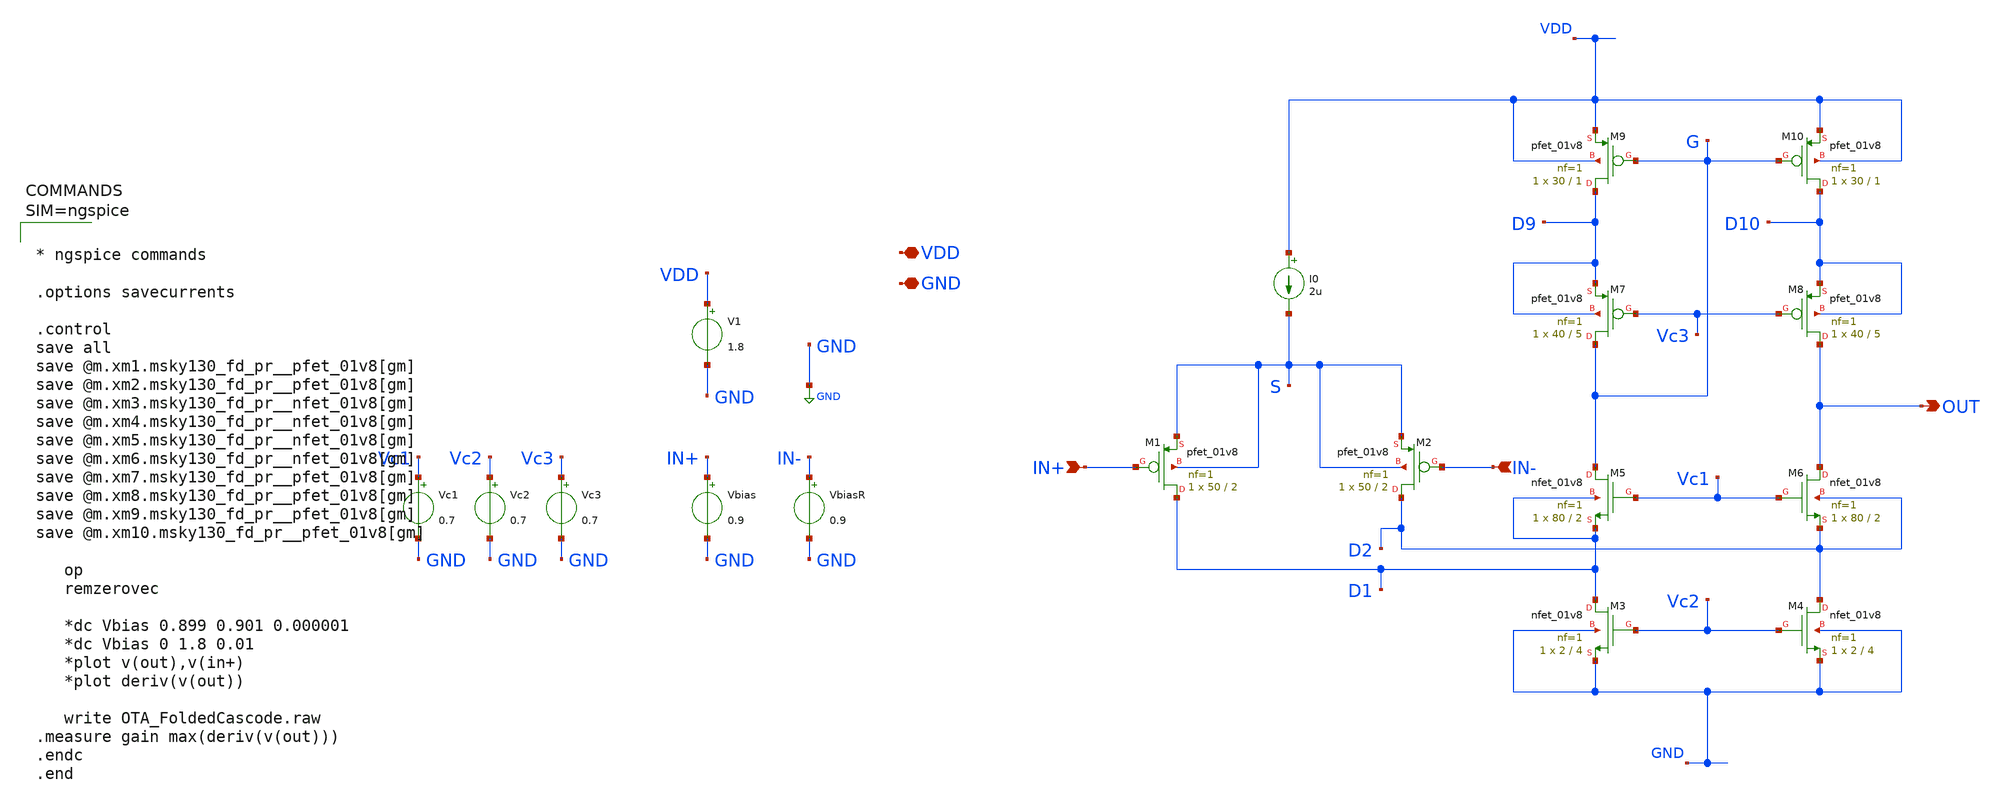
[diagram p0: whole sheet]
** sch_path: xschem/OTA_FoldedCascode.sch
**.subckt OTA_FoldedCascode VDD GND IN+ IN- OUT
*.iopin VDD
*.iopin GND
*.ipin IN+
*.ipin IN-
*.opin OUT
V1 VDD GND 1.8
Vbias IN+ GND 0.9
VbiasR IN- GND 0.9
I0 VDD S 2u
XM1 D1 IN+ S S sky130_fd_pr__pfet_01v8 L=2 W=50 nf=1 ad='int((nf+1)/2) * W/nf * 0.29' as='int((nf+2)/2) * W/nf * 0.29'
+ pd='2*int((nf+1)/2) * (W/nf + 0.29)' ps='2*int((nf+2)/2) * (W/nf + 0.29)' nrd='0.29 / W' nrs='0.29 / W'
+ sa=0 sb=0 sd=0 mult=1 m=1
XM2 D2 IN- S S sky130_fd_pr__pfet_01v8 L=2 W=50 nf=1 ad='int((nf+1)/2) * W/nf * 0.29' as='int((nf+2)/2) * W/nf * 0.29'
+ pd='2*int((nf+1)/2) * (W/nf + 0.29)' ps='2*int((nf+2)/2) * (W/nf + 0.29)' nrd='0.29 / W' nrs='0.29 / W'
+ sa=0 sb=0 sd=0 mult=1 m=1
XM3 D1 Vc2 GND GND sky130_fd_pr__nfet_01v8 L=4 W=2 nf=1 ad='int((nf+1)/2) * W/nf * 0.29' as='int((nf+2)/2) * W/nf * 0.29'
+ pd='2*int((nf+1)/2) * (W/nf + 0.29)' ps='2*int((nf+2)/2) * (W/nf + 0.29)' nrd='0.29 / W' nrs='0.29 / W'
+ sa=0 sb=0 sd=0 mult=1 m=1
XM4 D2 Vc2 GND GND sky130_fd_pr__nfet_01v8 L=4 W=2 nf=1 ad='int((nf+1)/2) * W/nf * 0.29' as='int((nf+2)/2) * W/nf * 0.29'
+ pd='2*int((nf+1)/2) * (W/nf + 0.29)' ps='2*int((nf+2)/2) * (W/nf + 0.29)' nrd='0.29 / W' nrs='0.29 / W'
+ sa=0 sb=0 sd=0 mult=1 m=1
XM5 G Vc1 D1 D1 sky130_fd_pr__nfet_01v8 L=2 W=80 nf=1 ad='int((nf+1)/2) * W/nf * 0.29' as='int((nf+2)/2) * W/nf * 0.29'
+ pd='2*int((nf+1)/2) * (W/nf + 0.29)' ps='2*int((nf+2)/2) * (W/nf + 0.29)' nrd='0.29 / W' nrs='0.29 / W'
+ sa=0 sb=0 sd=0 mult=1 m=1
XM6 OUT Vc1 D2 D2 sky130_fd_pr__nfet_01v8 L=2 W=80 nf=1 ad='int((nf+1)/2) * W/nf * 0.29' as='int((nf+2)/2) * W/nf * 0.29'
+ pd='2*int((nf+1)/2) * (W/nf + 0.29)' ps='2*int((nf+2)/2) * (W/nf + 0.29)' nrd='0.29 / W' nrs='0.29 / W'
+ sa=0 sb=0 sd=0 mult=1 m=1
XM7 G Vc3 D9 D9 sky130_fd_pr__pfet_01v8 L=5 W=40 nf=1 ad='int((nf+1)/2) * W/nf * 0.29' as='int((nf+2)/2) * W/nf * 0.29'
+ pd='2*int((nf+1)/2) * (W/nf + 0.29)' ps='2*int((nf+2)/2) * (W/nf + 0.29)' nrd='0.29 / W' nrs='0.29 / W'
+ sa=0 sb=0 sd=0 mult=1 m=1
XM8 OUT Vc3 D10 D10 sky130_fd_pr__pfet_01v8 L=5 W=40 nf=1 ad='int((nf+1)/2) * W/nf * 0.29' as='int((nf+2)/2) * W/nf * 0.29'
+ pd='2*int((nf+1)/2) * (W/nf + 0.29)' ps='2*int((nf+2)/2) * (W/nf + 0.29)' nrd='0.29 / W' nrs='0.29 / W'
+ sa=0 sb=0 sd=0 mult=1 m=1
XM9 D9 G VDD VDD sky130_fd_pr__pfet_01v8 L=1 W=30 nf=1 ad='int((nf+1)/2) * W/nf * 0.29' as='int((nf+2)/2) * W/nf * 0.29'
+ pd='2*int((nf+1)/2) * (W/nf + 0.29)' ps='2*int((nf+2)/2) * (W/nf + 0.29)' nrd='0.29 / W' nrs='0.29 / W'
+ sa=0 sb=0 sd=0 mult=1 m=1
XM10 D10 G VDD VDD sky130_fd_pr__pfet_01v8 L=1 W=30 nf=1 ad='int((nf+1)/2) * W/nf * 0.29' as='int((nf+2)/2) * W/nf * 0.29'
+ pd='2*int((nf+1)/2) * (W/nf + 0.29)' ps='2*int((nf+2)/2) * (W/nf + 0.29)' nrd='0.29 / W' nrs='0.29 / W'
+ sa=0 sb=0 sd=0 mult=1 m=1
Vc1 Vc1 GND 0.7
Vc2 Vc2 GND 0.7
Vc3 Vc3 GND 0.7
**** begin user architecture code



* ngspice commands

.options savecurrents

.control
save all
save @m.xm1.msky130_fd_pr__pfet_01v8[gm]
save @m.xm2.msky130_fd_pr__pfet_01v8[gm]
save @m.xm3.msky130_fd_pr__nfet_01v8[gm]
save @m.xm4.msky130_fd_pr__nfet_01v8[gm]
save @m.xm5.msky130_fd_pr__nfet_01v8[gm]
save @m.xm6.msky130_fd_pr__nfet_01v8[gm]
save @m.xm7.msky130_fd_pr__pfet_01v8[gm]
save @m.xm8.msky130_fd_pr__pfet_01v8[gm]
save @m.xm9.msky130_fd_pr__pfet_01v8[gm]
save @m.xm10.msky130_fd_pr__pfet_01v8[gm]

   op
   remzerovec

   *dc Vbias 0.899 0.901 0.000001
   *dc Vbias 0 1.8 0.01
   *plot v(out),v(in+)
   *plot deriv(v(out))

   write OTA_FoldedCascode.raw
.measure gain max(deriv(v(out)))
.endc
.end



.lib $::SKYWATER_MODELS/sky130.lib.spice tt
**** end user architecture code
**.ends
.GLOBAL GND
.end
